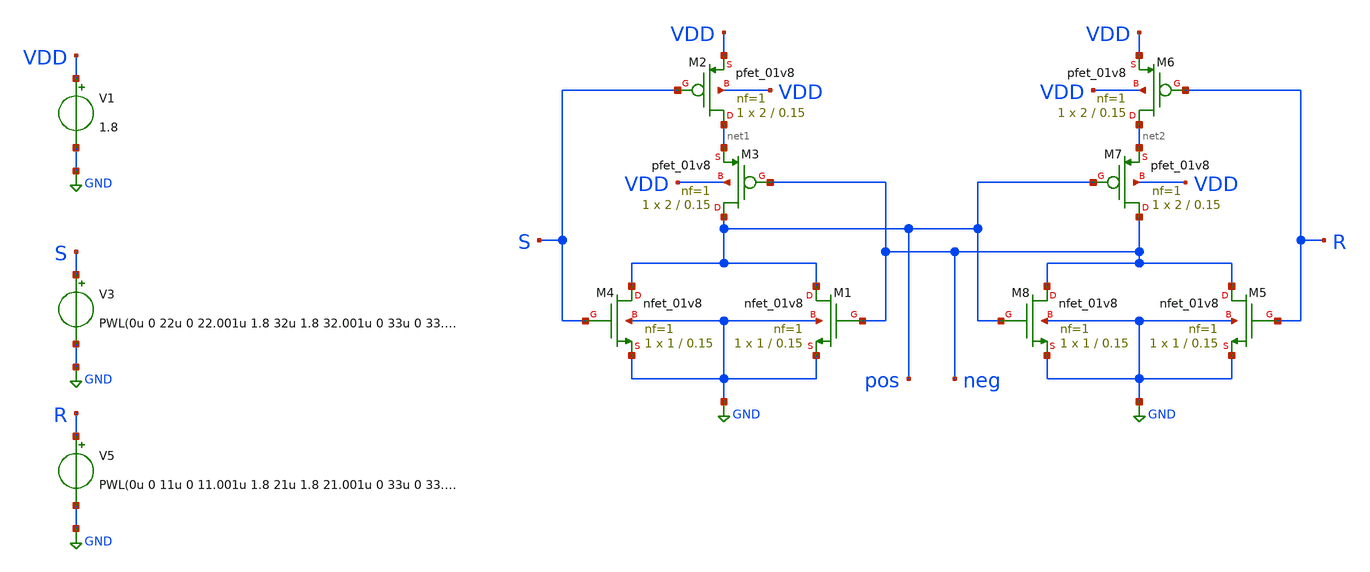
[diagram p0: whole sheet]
** sch_path: schem/sr_latch.sch
**.subckt sr_latch
XM1 pos neg GND GND sky130_fd_pr__nfet_01v8 L=0.15 W=1 nf=1 ad='int((1 + 1)/2) * 1 / 1 * 0.29' as='int((1 + 2)/2) * 1 / 1 * 0.29'
+ pd='2*int((1 + 1)/2) * (1 / 1 + 0.29)' ps='2*int((1 + 2)/2) * (1 / 1 + 0.29)' nrd='0.29 / 1 ' nrs='0.29 / 1 '
+ sa=0 sb=0 sd=0 mult=1 m=1
XM2 net1 S VDD VDD sky130_fd_pr__pfet_01v8 L=0.15 W=2 nf=1 ad='int((1 + 1)/2) * 2 / 1 * 0.29' as='int((1 + 2)/2) * 2 / 1 * 0.29'
+ pd='2*int((1 + 1)/2) * (2 / 1 + 0.29)' ps='2*int((1 + 2)/2) * (2 / 1 + 0.29)' nrd='0.29 / 2 ' nrs='0.29 / 2 '
+ sa=0 sb=0 sd=0 mult=1 m=1
XM3 pos neg net1 VDD sky130_fd_pr__pfet_01v8 L=0.15 W=2 nf=1 ad='int((1 + 1)/2) * 2 / 1 * 0.29' as='int((1 + 2)/2) * 2 / 1 * 0.29'
+ pd='2*int((1 + 1)/2) * (2 / 1 + 0.29)' ps='2*int((1 + 2)/2) * (2 / 1 + 0.29)' nrd='0.29 / 2 ' nrs='0.29 / 2 '
+ sa=0 sb=0 sd=0 mult=1 m=1
XM4 pos S GND GND sky130_fd_pr__nfet_01v8 L=0.15 W=1 nf=1 ad='int((1 + 1)/2) * 1 / 1 * 0.29' as='int((1 + 2)/2) * 1 / 1 * 0.29'
+ pd='2*int((1 + 1)/2) * (1 / 1 + 0.29)' ps='2*int((1 + 2)/2) * (1 / 1 + 0.29)' nrd='0.29 / 1 ' nrs='0.29 / 1 '
+ sa=0 sb=0 sd=0 mult=1 m=1
XM5 neg R GND GND sky130_fd_pr__nfet_01v8 L=0.15 W=1 nf=1 ad='int((1 + 1)/2) * 1 / 1 * 0.29' as='int((1 + 2)/2) * 1 / 1 * 0.29'
+ pd='2*int((1 + 1)/2) * (1 / 1 + 0.29)' ps='2*int((1 + 2)/2) * (1 / 1 + 0.29)' nrd='0.29 / 1 ' nrs='0.29 / 1 '
+ sa=0 sb=0 sd=0 mult=1 m=1
XM6 net2 R VDD VDD sky130_fd_pr__pfet_01v8 L=0.15 W=2 nf=1 ad='int((1 + 1)/2) * 2 / 1 * 0.29' as='int((1 + 2)/2) * 2 / 1 * 0.29'
+ pd='2*int((1 + 1)/2) * (2 / 1 + 0.29)' ps='2*int((1 + 2)/2) * (2 / 1 + 0.29)' nrd='0.29 / 2 ' nrs='0.29 / 2 '
+ sa=0 sb=0 sd=0 mult=1 m=1
XM7 neg pos net2 VDD sky130_fd_pr__pfet_01v8 L=0.15 W=2 nf=1 ad='int((1 + 1)/2) * 2 / 1 * 0.29' as='int((1 + 2)/2) * 2 / 1 * 0.29'
+ pd='2*int((1 + 1)/2) * (2 / 1 + 0.29)' ps='2*int((1 + 2)/2) * (2 / 1 + 0.29)' nrd='0.29 / 2 ' nrs='0.29 / 2 '
+ sa=0 sb=0 sd=0 mult=1 m=1
XM8 neg pos GND GND sky130_fd_pr__nfet_01v8 L=0.15 W=1 nf=1 ad='int((1 + 1)/2) * 1 / 1 * 0.29' as='int((1 + 2)/2) * 1 / 1 * 0.29'
+ pd='2*int((1 + 1)/2) * (1 / 1 + 0.29)' ps='2*int((1 + 2)/2) * (1 / 1 + 0.29)' nrd='0.29 / 1 ' nrs='0.29 / 1 '
+ sa=0 sb=0 sd=0 mult=1 m=1
V1 VDD GND 1.8
V3 S GND PWL(0u 0 22u 0 22.001u 1.8 32u 1.8 32.001u 0 33u 0 33.001u 1.8 43u 1.8 43.001u 0 44u 0)
V5 R GND PWL(0u 0 11u 0 11.001u 1.8 21u 1.8 21.001u 0 33u 0 33.001u 1.8 43u 1.8 43.001u 0 44u 0)
**** begin user architecture code


.lib /usr/local/share/pdk/sky130A/libs.tech/ngspice/sky130.lib.spice tt

.tran 10n 45u
.save all

.control
    run
    plot S R pos neg
.endc

.end


**** end user architecture code
**.ends
.GLOBAL GND
.end
